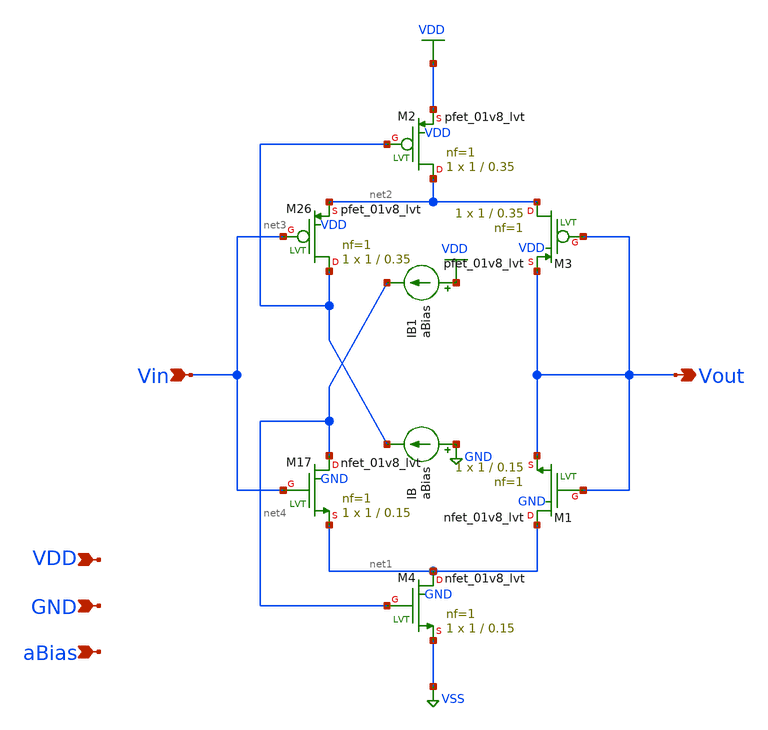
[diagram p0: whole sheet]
** sch_path: Voltage_Buffer.sch
**.subckt Voltage_Buffer Vin Vout VDD GND aBias
*.ipin Vin
*.opin Vout
*.ipin VDD
*.ipin GND
*.ipin aBias
IB GND net3 aBias
IB1 VDD net4 aBias
XM26 net3 Vin net2 VDD sky130_fd_pr__pfet_01v8_lvt L=0.35 W=1 nf=1 ad='int((1 + 1)/2) * 1 / 1 * 0.29'
+ as='int((1 + 2)/2) * 1 / 1 * 0.29' pd='2*int((1 + 1)/2) * (1 / 1 + 0.29)' ps='2*int((1 + 2)/2) * (1 / 1 + 0.29)'
+ nrd='0.29 / 1 ' nrs='0.29 / 1 ' sa=0 sb=0 sd=0 mult=1 m=1
XM17 net4 Vin net1 GND sky130_fd_pr__nfet_01v8_lvt L=0.15 W=1 nf=1 ad='int((1 + 1)/2) * 1 / 1 * 0.29'
+ as='int((1 + 2)/2) * 1 / 1 * 0.29' pd='2*int((1 + 1)/2) * (1 / 1 + 0.29)' ps='2*int((1 + 2)/2) * (1 / 1 + 0.29)'
+ nrd='0.29 / 1 ' nrs='0.29 / 1 ' sa=0 sb=0 sd=0 mult=1 m=1
XM1 net1 Vout Vout GND sky130_fd_pr__nfet_01v8_lvt L=0.15 W=1 nf=1 ad='int((1 + 1)/2) * 1 / 1 * 0.29'
+ as='int((1 + 2)/2) * 1 / 1 * 0.29' pd='2*int((1 + 1)/2) * (1 / 1 + 0.29)' ps='2*int((1 + 2)/2) * (1 / 1 + 0.29)'
+ nrd='0.29 / 1 ' nrs='0.29 / 1 ' sa=0 sb=0 sd=0 mult=1 m=1
XM4 net1 net4 VSS GND sky130_fd_pr__nfet_01v8_lvt L=0.15 W=1 nf=1 ad='int((1 + 1)/2) * 1 / 1 * 0.29'
+ as='int((1 + 2)/2) * 1 / 1 * 0.29' pd='2*int((1 + 1)/2) * (1 / 1 + 0.29)' ps='2*int((1 + 2)/2) * (1 / 1 + 0.29)'
+ nrd='0.29 / 1 ' nrs='0.29 / 1 ' sa=0 sb=0 sd=0 mult=1 m=1
XM2 net2 net3 VDD VDD sky130_fd_pr__pfet_01v8_lvt L=0.35 W=1 nf=1 ad='int((1 + 1)/2) * 1 / 1 * 0.29'
+ as='int((1 + 2)/2) * 1 / 1 * 0.29' pd='2*int((1 + 1)/2) * (1 / 1 + 0.29)' ps='2*int((1 + 2)/2) * (1 / 1 + 0.29)'
+ nrd='0.29 / 1 ' nrs='0.29 / 1 ' sa=0 sb=0 sd=0 mult=1 m=1
XM3 net2 Vout Vout VDD sky130_fd_pr__pfet_01v8_lvt L=0.35 W=1 nf=1 ad='int((1 + 1)/2) * 1 / 1 * 0.29'
+ as='int((1 + 2)/2) * 1 / 1 * 0.29' pd='2*int((1 + 1)/2) * (1 / 1 + 0.29)' ps='2*int((1 + 2)/2) * (1 / 1 + 0.29)'
+ nrd='0.29 / 1 ' nrs='0.29 / 1 ' sa=0 sb=0 sd=0 mult=1 m=1
**.ends
.GLOBAL VDD
.GLOBAL VSS
.GLOBAL GND
.end
